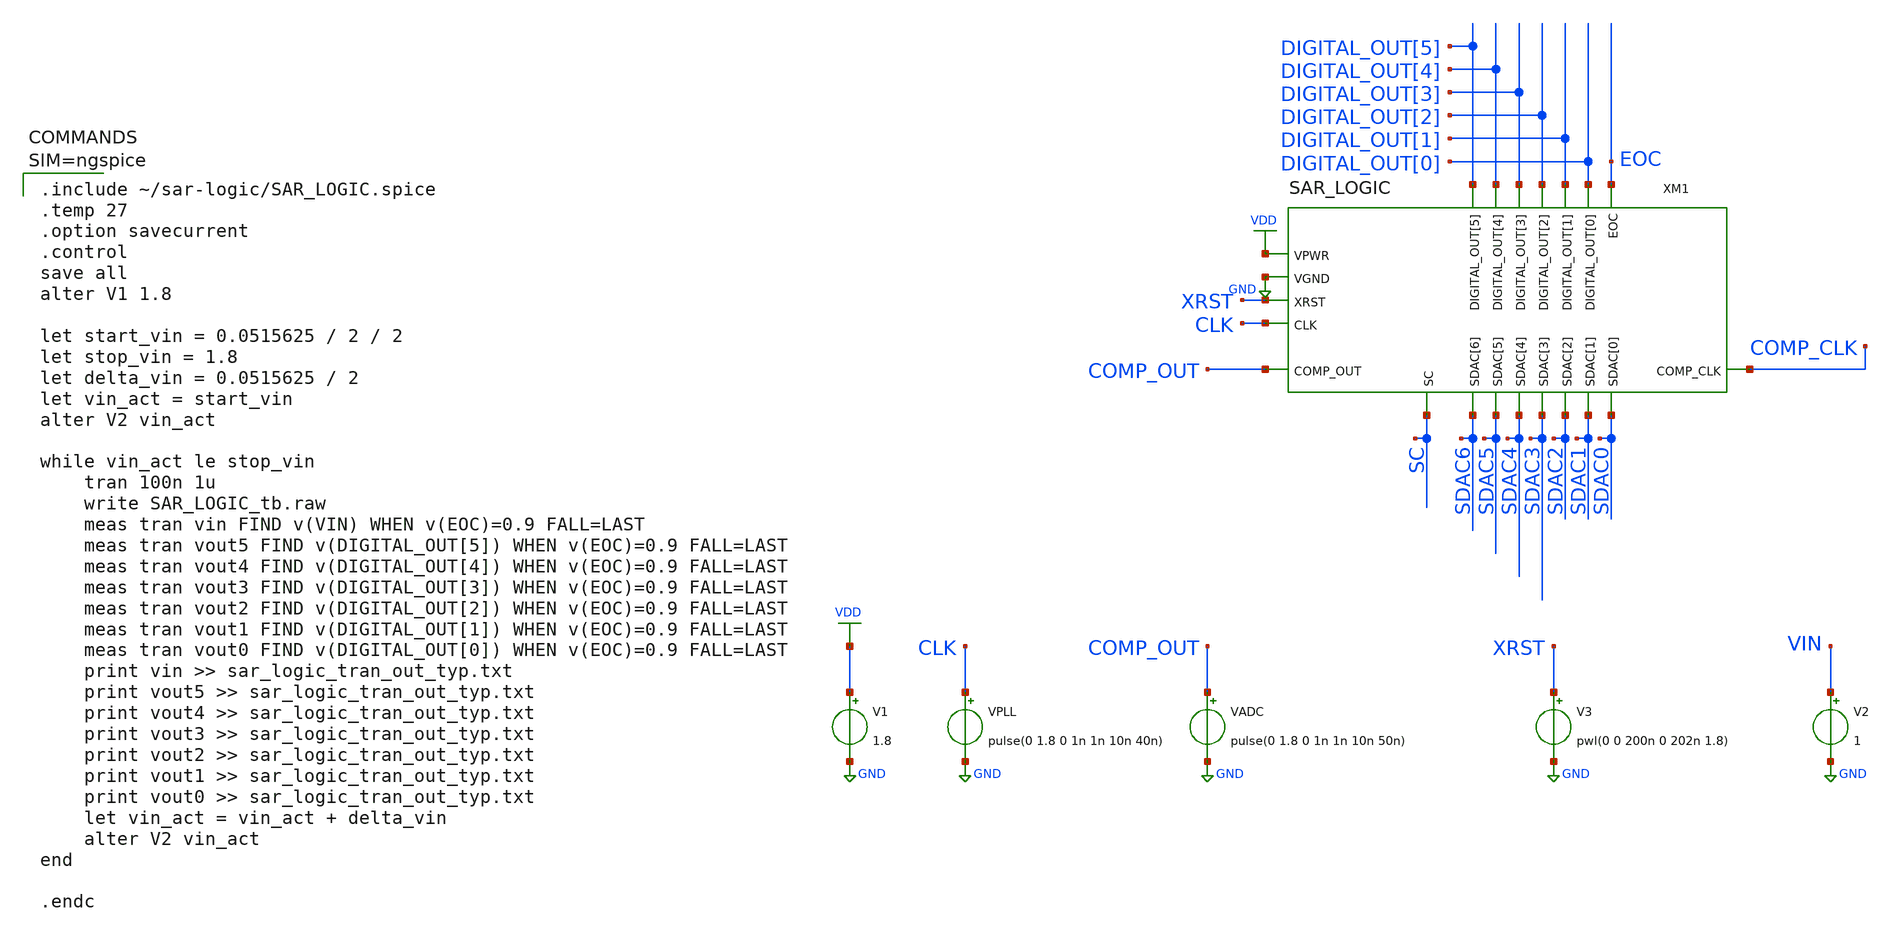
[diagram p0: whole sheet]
** sch_path: SKY130/SAR-ADC/SAR-ADC_1.8V/SAR_LOGIC_tb.sch
**.subckt SAR_LOGIC_tb
XM1 CLK COMP_CLK COMP_OUT DIGITAL_OUT[0] DIGITAL_OUT[1] DIGITAL_OUT[2] DIGITAL_OUT[3] DIGITAL_OUT[4]
+ DIGITAL_OUT[5] EOC SC SDAC0 SDAC1 SDAC2 SDAC3 SDAC4 SDAC5 SDAC6 GND VDD XRST SAR_LOGIC
V1 VDD GND 1.8
VPLL CLK GND pulse(0 1.8 0 1n 1n 10n 40n)
V3 XRST GND pwl(0 0 200n 0 202n 1.8)
V2 VIN GND 1
VADC COMP_OUT GND pulse(0 1.8 0 1n 1n 10n 50n)
**** begin user architecture code

** opencircuitdesign pdks install
.lib $::SKYWATER_MODELS/sky130.lib.spice tt



.include ~/sar-logic/SAR_LOGIC.spice
.temp 27
.option savecurrent
.control
save all
alter V1 1.8

let start_vin = 0.0515625 / 2 / 2
let stop_vin = 1.8
let delta_vin = 0.0515625 / 2
let vin_act = start_vin
alter V2 vin_act

while vin_act le stop_vin
	tran 100n 1u
	write SAR_LOGIC_tb.raw
	meas tran vin FIND v(VIN) WHEN v(EOC)=0.9 FALL=LAST
	meas tran vout5 FIND v(DIGITAL_OUT[5]) WHEN v(EOC)=0.9 FALL=LAST
	meas tran vout4 FIND v(DIGITAL_OUT[4]) WHEN v(EOC)=0.9 FALL=LAST
	meas tran vout3 FIND v(DIGITAL_OUT[3]) WHEN v(EOC)=0.9 FALL=LAST
	meas tran vout2 FIND v(DIGITAL_OUT[2]) WHEN v(EOC)=0.9 FALL=LAST
	meas tran vout1 FIND v(DIGITAL_OUT[1]) WHEN v(EOC)=0.9 FALL=LAST
	meas tran vout0 FIND v(DIGITAL_OUT[0]) WHEN v(EOC)=0.9 FALL=LAST
	print vin >> sar_logic_tran_out_typ.txt
	print vout5 >> sar_logic_tran_out_typ.txt
	print vout4 >> sar_logic_tran_out_typ.txt
	print vout3 >> sar_logic_tran_out_typ.txt
	print vout2 >> sar_logic_tran_out_typ.txt
	print vout1 >> sar_logic_tran_out_typ.txt
	print vout0 >> sar_logic_tran_out_typ.txt
	let vin_act = vin_act + delta_vin
	alter V2 vin_act
end

.endc



**** end user architecture code
**.ends
.GLOBAL GND
.GLOBAL VDD
.end
